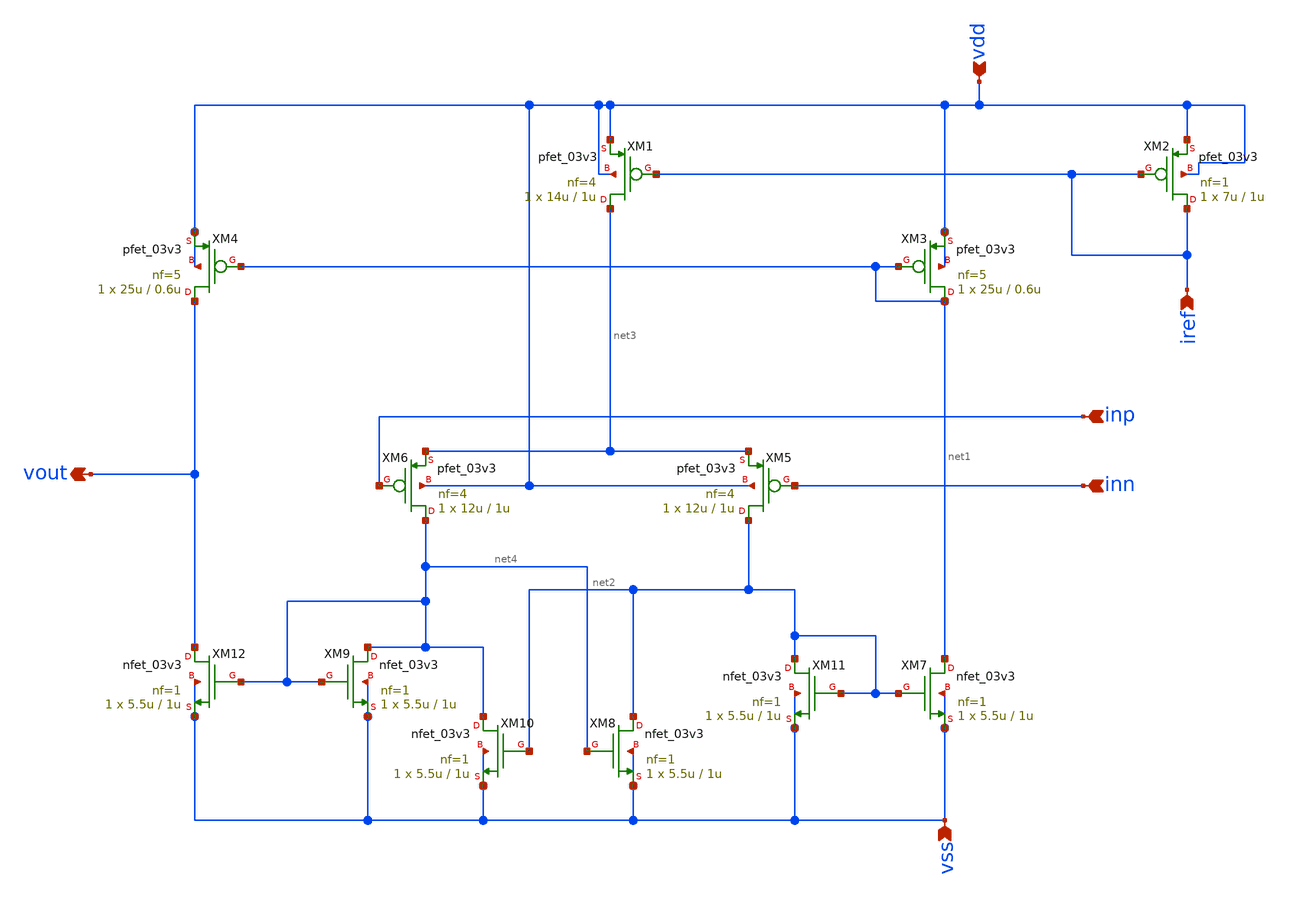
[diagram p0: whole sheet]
** sch_path: designs/libs/core_analog/Comparator/Pmos_Comparator.sch
**.subckt Pmos_Comparator vdd vss iref inn inp vout
*.ipin vdd
*.ipin vss
*.ipin iref
*.ipin inn
*.ipin inp
*.opin vout
XM3 net1 net1 vdd vdd pfet_03v3 L=0.6u W=25u nf=5 ad='int((nf+1)/2) * W/nf * 0.18u' as='int((nf+2)/2) * W/nf * 0.18u'
+ pd='2*int((nf+1)/2) * (W/nf + 0.18u)' ps='2*int((nf+2)/2) * (W/nf + 0.18u)' nrd='0.18u / W' nrs='0.18u / W'
+ sa=0 sb=0 sd=0 m=1
XM4 vout net1 vdd vdd pfet_03v3 L=0.6u W=25u nf=5 ad='int((nf+1)/2) * W/nf * 0.18u' as='int((nf+2)/2) * W/nf * 0.18u'
+ pd='2*int((nf+1)/2) * (W/nf + 0.18u)' ps='2*int((nf+2)/2) * (W/nf + 0.18u)' nrd='0.18u / W' nrs='0.18u / W'
+ sa=0 sb=0 sd=0 m=1
XM5 net2 inn net3 vdd pfet_03v3 L=1u W=12u nf=4 ad='int((nf+1)/2) * W/nf * 0.18u' as='int((nf+2)/2) * W/nf * 0.18u'
+ pd='2*int((nf+1)/2) * (W/nf + 0.18u)' ps='2*int((nf+2)/2) * (W/nf + 0.18u)' nrd='0.18u / W' nrs='0.18u / W'
+ sa=0 sb=0 sd=0 m=1
XM6 net4 inp net3 vdd pfet_03v3 L=1u W=12u nf=4 ad='int((nf+1)/2) * W/nf * 0.18u' as='int((nf+2)/2) * W/nf * 0.18u'
+ pd='2*int((nf+1)/2) * (W/nf + 0.18u)' ps='2*int((nf+2)/2) * (W/nf + 0.18u)' nrd='0.18u / W' nrs='0.18u / W'
+ sa=0 sb=0 sd=0 m=1
XM7 net1 net2 vss vss nfet_03v3 L=1u W=5.5u nf=1 ad='int((nf+1)/2) * W/nf * 0.18u' as='int((nf+2)/2) * W/nf * 0.18u'
+ pd='2*int((nf+1)/2) * (W/nf + 0.18u)' ps='2*int((nf+2)/2) * (W/nf + 0.18u)' nrd='0.18u / W' nrs='0.18u / W'
+ sa=0 sb=0 sd=0 m=1
XM8 net2 net4 vss vss nfet_03v3 L=1u W=5.5u nf=1 ad='int((nf+1)/2) * W/nf * 0.18u' as='int((nf+2)/2) * W/nf * 0.18u'
+ pd='2*int((nf+1)/2) * (W/nf + 0.18u)' ps='2*int((nf+2)/2) * (W/nf + 0.18u)' nrd='0.18u / W' nrs='0.18u / W'
+ sa=0 sb=0 sd=0 m=1
XM9 net4 net4 vss vss nfet_03v3 L=1u W=5.5u nf=1 ad='int((nf+1)/2) * W/nf * 0.18u' as='int((nf+2)/2) * W/nf * 0.18u'
+ pd='2*int((nf+1)/2) * (W/nf + 0.18u)' ps='2*int((nf+2)/2) * (W/nf + 0.18u)' nrd='0.18u / W' nrs='0.18u / W'
+ sa=0 sb=0 sd=0 m=1
XM10 net4 net2 vss vss nfet_03v3 L=1u W=5.5u nf=1 ad='int((nf+1)/2) * W/nf * 0.18u' as='int((nf+2)/2) * W/nf * 0.18u'
+ pd='2*int((nf+1)/2) * (W/nf + 0.18u)' ps='2*int((nf+2)/2) * (W/nf + 0.18u)' nrd='0.18u / W' nrs='0.18u / W'
+ sa=0 sb=0 sd=0 m=1
XM11 net2 net2 vss vss nfet_03v3 L=1u W=5.5u nf=1 ad='int((nf+1)/2) * W/nf * 0.18u' as='int((nf+2)/2) * W/nf * 0.18u'
+ pd='2*int((nf+1)/2) * (W/nf + 0.18u)' ps='2*int((nf+2)/2) * (W/nf + 0.18u)' nrd='0.18u / W' nrs='0.18u / W'
+ sa=0 sb=0 sd=0 m=1
XM12 vout net4 vss vss nfet_03v3 L=1u W=5.5u nf=1 ad='int((nf+1)/2) * W/nf * 0.18u' as='int((nf+2)/2) * W/nf * 0.18u'
+ pd='2*int((nf+1)/2) * (W/nf + 0.18u)' ps='2*int((nf+2)/2) * (W/nf + 0.18u)' nrd='0.18u / W' nrs='0.18u / W'
+ sa=0 sb=0 sd=0 m=1
XM1 net3 iref vdd vdd pfet_03v3 L=1u W=14u nf=4 ad='int((nf+1)/2) * W/nf * 0.18u' as='int((nf+2)/2) * W/nf * 0.18u'
+ pd='2*int((nf+1)/2) * (W/nf + 0.18u)' ps='2*int((nf+2)/2) * (W/nf + 0.18u)' nrd='0.18u / W' nrs='0.18u / W'
+ sa=0 sb=0 sd=0 m=1
XM2 iref iref vdd vdd pfet_03v3 L=1u W=7u nf=1 ad='int((nf+1)/2) * W/nf * 0.18u' as='int((nf+2)/2) * W/nf * 0.18u'
+ pd='2*int((nf+1)/2) * (W/nf + 0.18u)' ps='2*int((nf+2)/2) * (W/nf + 0.18u)' nrd='0.18u / W' nrs='0.18u / W'
+ sa=0 sb=0 sd=0 m=1
**.ends
.end
